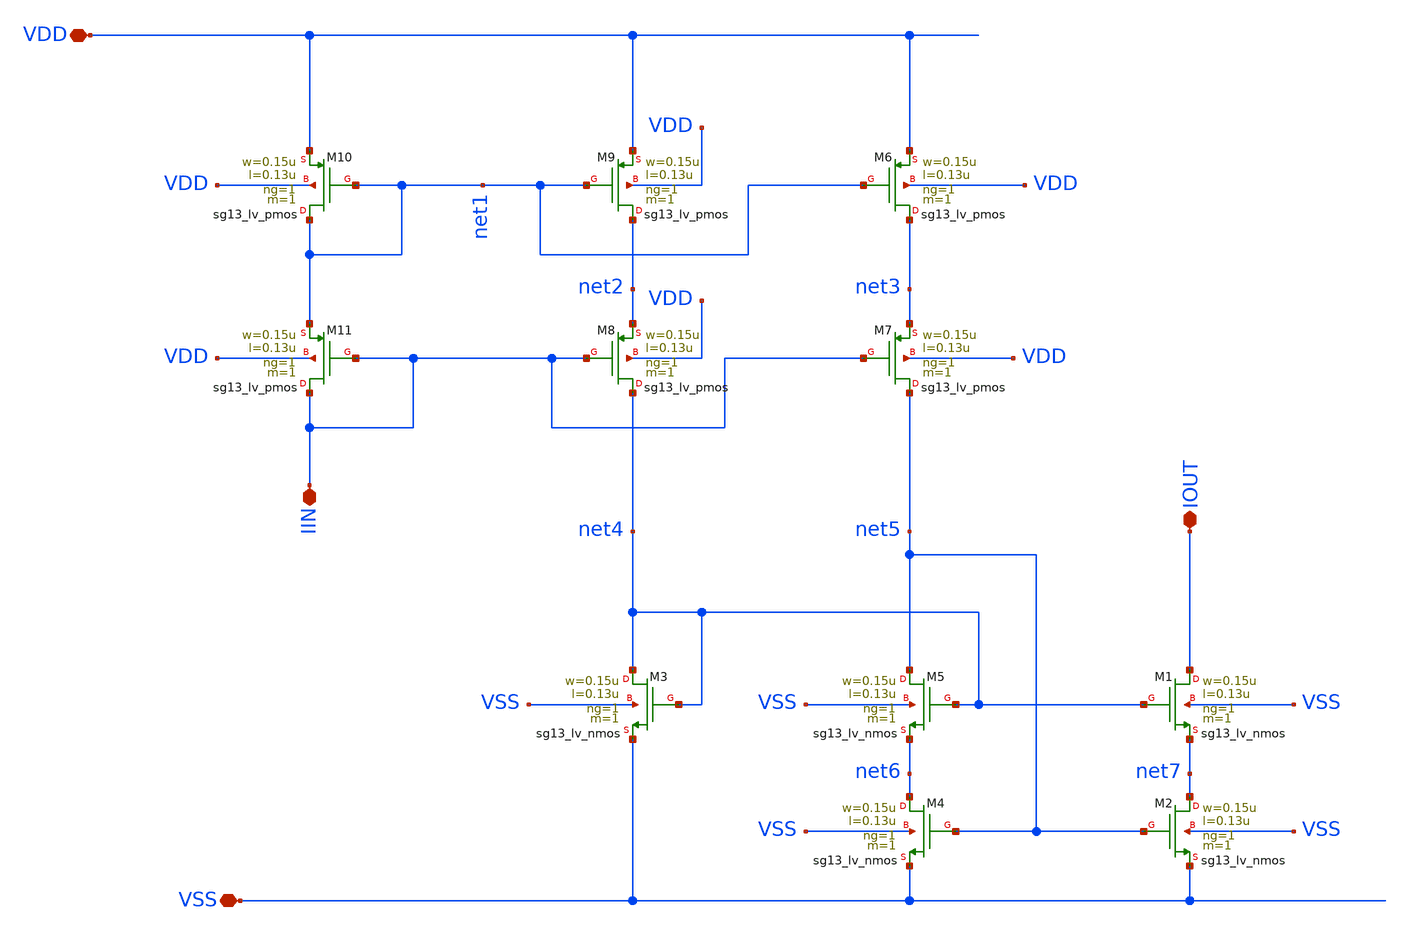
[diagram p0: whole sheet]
** sch_path: analog-db/templates/current_mirror/nmos_current_sink/wide_swing_current_mirror_nmos.sch
**.subckt wide_swing_current_mirror_nmos VDD IIN VSS IOUT
*.iopin VDD
*.iopin IIN
*.iopin VSS
*.iopin IOUT
XM1 IOUT net4 net7 VSS sg13_lv_nmos w=0.15u l=0.13u ng=1 m=1 mm_ok=1
XM2 net7 net5 VSS VSS sg13_lv_nmos w=0.15u l=0.13u ng=1 m=1 mm_ok=1
XM3 net4 net4 VSS VSS sg13_lv_nmos w=0.15u l=0.13u ng=1 m=1 mm_ok=1
XM4 net6 net5 VSS VSS sg13_lv_nmos w=0.15u l=0.13u ng=1 m=1 mm_ok=1
XM5 net5 net4 net6 VSS sg13_lv_nmos w=0.15u l=0.13u ng=1 m=1 mm_ok=1
XM6 net3 net1 VDD VDD sg13_lv_pmos w=0.15u l=0.13u ng=1 m=1 mm_ok=1
XM7 net5 IIN net3 VDD sg13_lv_pmos w=0.15u l=0.13u ng=1 m=1 mm_ok=1
XM8 net4 IIN net2 VDD sg13_lv_pmos w=0.15u l=0.13u ng=1 m=1 mm_ok=1
XM9 net2 net1 VDD VDD sg13_lv_pmos w=0.15u l=0.13u ng=1 m=1 mm_ok=1
XM10 net1 net1 VDD VDD sg13_lv_pmos w=0.15u l=0.13u ng=1 m=1 mm_ok=1
XM11 IIN IIN net1 VDD sg13_lv_pmos w=0.15u l=0.13u ng=1 m=1 mm_ok=1
**.ends
.end
